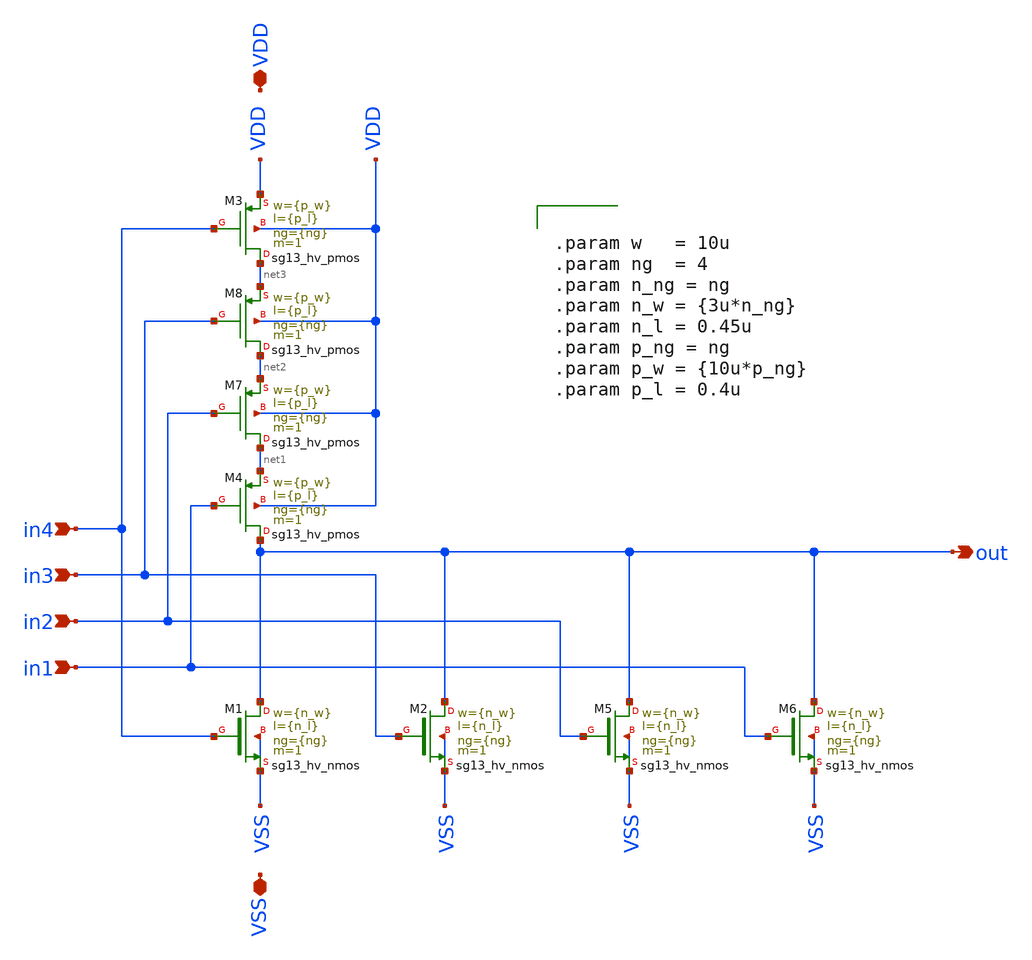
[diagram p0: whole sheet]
** sch_path: macros/heichips26_vcr/macros/switched_capacitor/schematic/xschem/hv_nor4.sch
**.subckt hv_nor4 in1 VDD VSS out in2 in3 in4
*.ipin in1
*.iopin VDD
*.iopin VSS
*.opin out
*.ipin in2
*.ipin in3
*.ipin in4
XM2 out in3 VSS VSS sg13_hv_nmos w={n_w} l={n_l} ng={ng} m=1 mm_ok=1
XM3 net3 in4 VDD VDD sg13_hv_pmos w={p_w} l={p_l} ng={ng} m=1 mm_ok=1
XM1 out in4 VSS VSS sg13_hv_nmos w={n_w} l={n_l} ng={ng} m=1 mm_ok=1
XM4 out in1 net1 VDD sg13_hv_pmos w={p_w} l={p_l} ng={ng} m=1 mm_ok=1
XM5 out in2 VSS VSS sg13_hv_nmos w={n_w} l={n_l} ng={ng} m=1 mm_ok=1
XM6 out in1 VSS VSS sg13_hv_nmos w={n_w} l={n_l} ng={ng} m=1 mm_ok=1
XM7 net1 in2 net2 VDD sg13_hv_pmos w={p_w} l={p_l} ng={ng} m=1 mm_ok=1
XM8 net2 in3 net3 VDD sg13_hv_pmos w={p_w} l={p_l} ng={ng} m=1 mm_ok=1
**** begin user architecture code


.param w   = 10u
.param ng  = 4
.param n_ng = ng
.param n_w = {3u*n_ng}
.param n_l = 0.45u
.param p_ng = ng
.param p_w = {10u*p_ng}
.param p_l = 0.4u


**** end user architecture code
**.ends
.end
